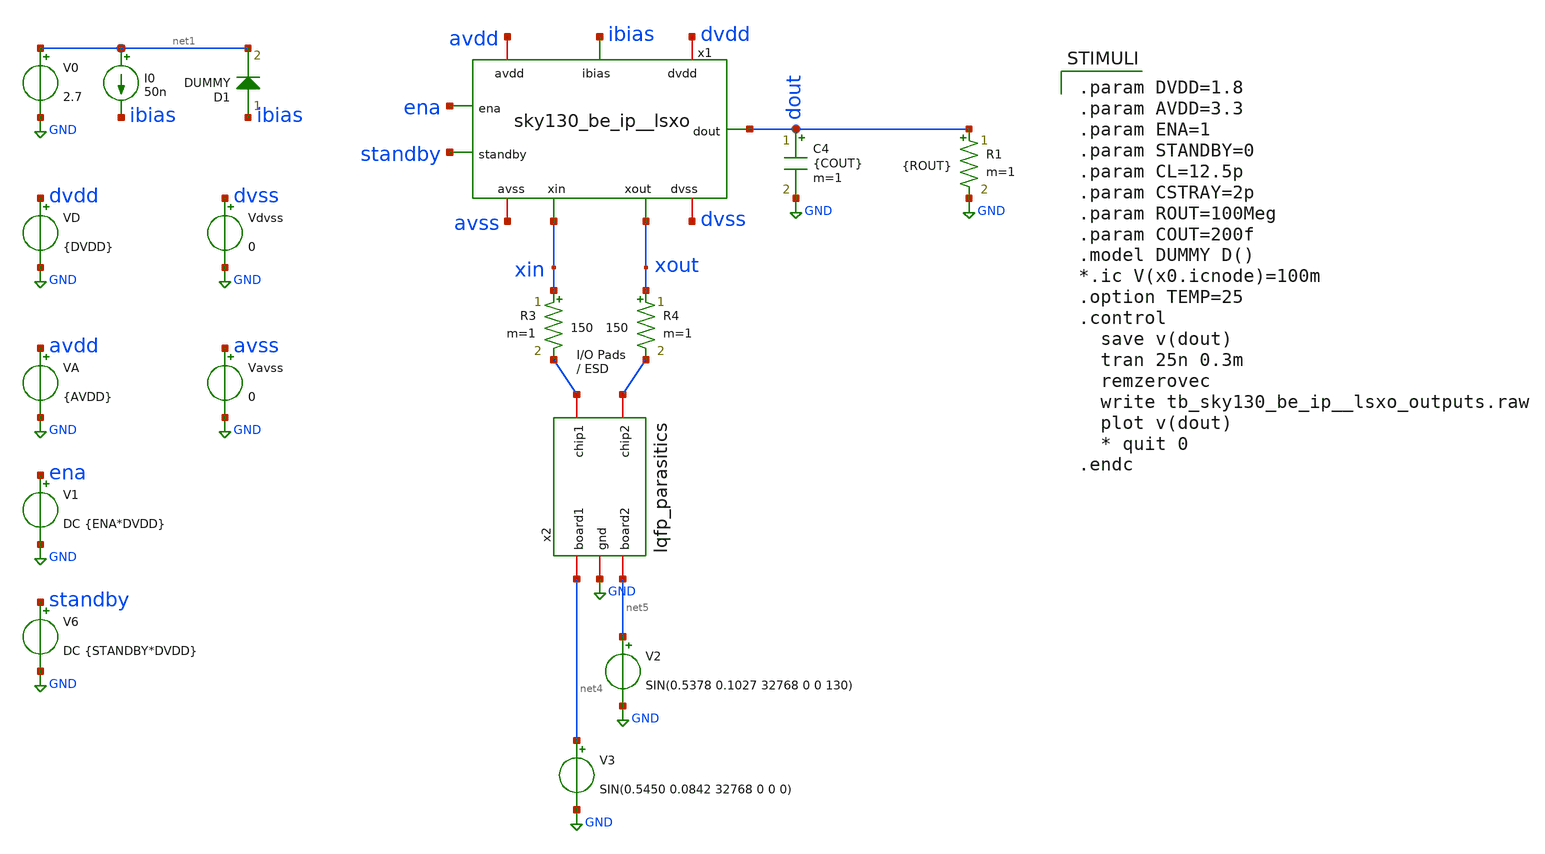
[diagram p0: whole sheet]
** sch_path: xschem/tb_sky130_be_ip__lsxo_outputs.sch

.lib $::SKYWATER_MODELS/sky130.lib.spice tt
.include $::SKYWATER_STDCELLS/sky130_fd_sc_hd.spice

**.subckt tb_sky130_be_ip__lsxo_outputs
VD dvdd GND {DVDD}
VA avdd GND {AVDD}
I0 net1 ibias 50n
C4 dout GND {COUT} m=1
V0 net1 GND 2.7
V6 standby GND DC {STANDBY*DVDD}
R3 xin net2 150 m=1
R4 xout net3 150 m=1
x2 net3 net2 GND net4 net5 lqfp_parasitics
V1 ena GND DC {ENA*DVDD}
D1 ibias net1 DUMMY area=100
x1 avdd avss dvdd dvss ibias ena standby dout xin xout sky130_be_ip__lsxo
V2 net5 GND SIN(0.5378 0.1027 32768 0 0 130)
V3 net4 GND SIN(0.5450 0.0842 32768 0 0 0)
R1 dout GND {ROUT} m=1
Vdvss dvss GND 0
Vavss avss GND 0
**** begin user architecture code

.param DVDD=1.8
.param AVDD=3.3
.param ENA=1
.param STANDBY=0
.param CL=12.5p
.param CSTRAY=2p
.param ROUT=100Meg
.param COUT=200f
.model DUMMY D()
*.ic V(x0.icnode)=100m
.option TEMP=25
.control
  save v(dout)
  tran 25n 0.3m
  remzerovec
  write tb_sky130_be_ip__lsxo_outputs.raw
  plot v(dout)
  * quit 0
.endc

**** end user architecture code
**.ends
.GLOBAL GND
.end
